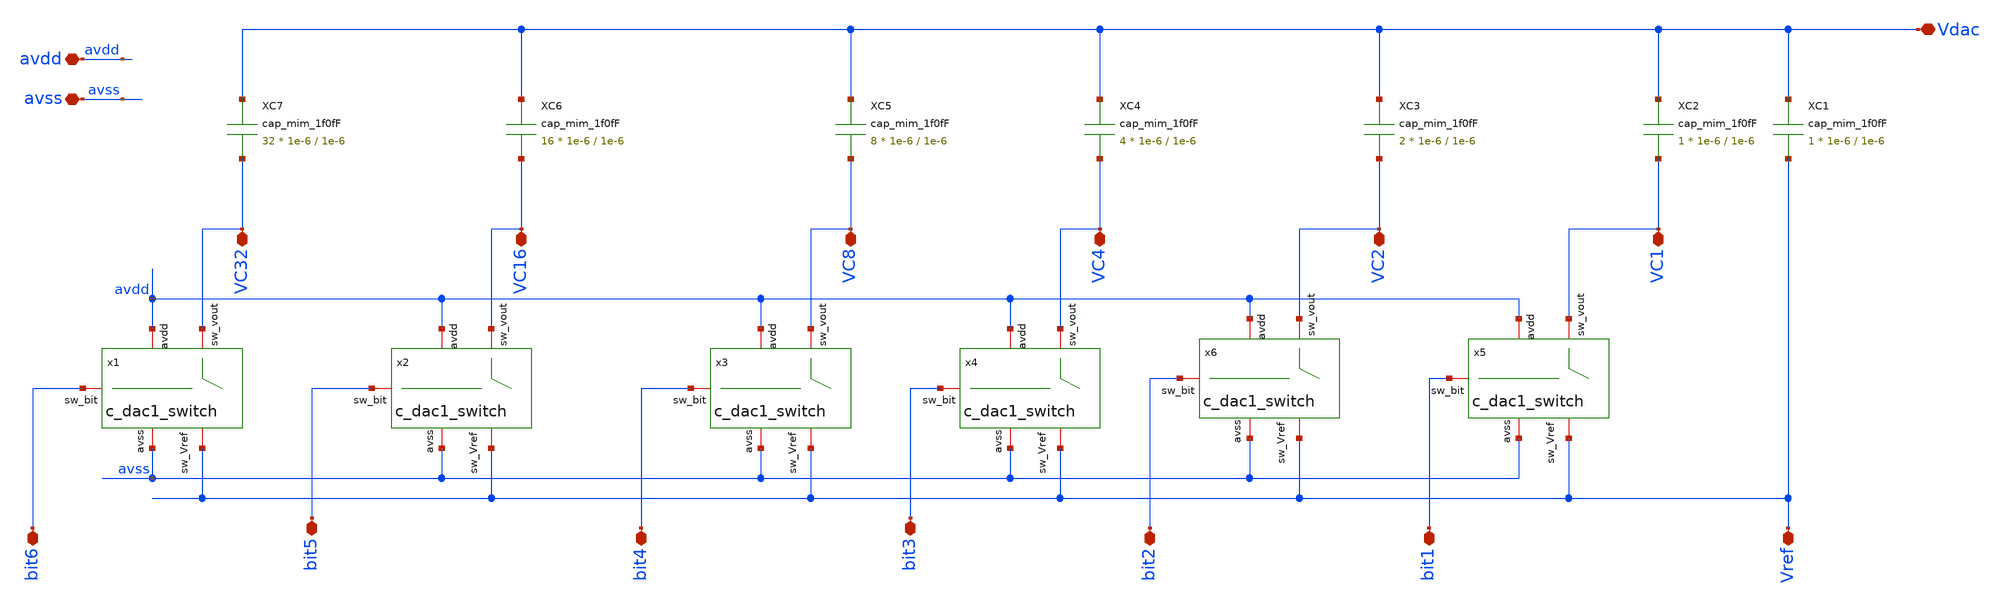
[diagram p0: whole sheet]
** sch_path: designs/libs/WK_Kadam/c_dac_v1.sch
**.subckt c_dac_v1 Vref VC1 VC2 VC4 VC8 VC16 VC32 Vdac avdd avss bit6 bit5 bit4 bit3 bit2 bit1
*.iopin Vref
*.iopin VC1
*.iopin VC2
*.iopin VC4
*.iopin VC8
*.iopin VC16
*.iopin VC32
*.iopin Vdac
*.iopin avdd
*.iopin avss
*.iopin bit6
*.iopin bit5
*.iopin bit4
*.iopin bit3
*.iopin bit2
*.iopin bit1
XC1 Vdac Vref cap_mim_1f0fF c_width=1e-6 c_length=1e-6 m=1
XC2 Vdac VC1 cap_mim_1f0fF c_width=1e-6 c_length=1e-6 m=1
XC3 Vdac VC2 cap_mim_1f0fF c_width=1e-6 c_length=1e-6 m=2
XC4 Vdac VC4 cap_mim_1f0fF c_width=1e-6 c_length=1e-6 m=4
XC5 Vdac VC8 cap_mim_1f0fF c_width=1e-6 c_length=1e-6 m=8
XC6 Vdac VC16 cap_mim_1f0fF c_width=1e-6 c_length=1e-6 m=16
XC7 Vdac VC32 cap_mim_1f0fF c_width=1e-6 c_length=1e-6 m=32
x1 avdd avss VC32 bit6 Vref c_dac1_switch
x2 avdd avss VC16 bit5 Vref c_dac1_switch
x3 avdd avss VC8 bit4 Vref c_dac1_switch
x4 avdd avss VC4 bit3 Vref c_dac1_switch
x5 avdd avss VC1 bit1 Vref c_dac1_switch
x6 avdd avss VC2 bit2 Vref c_dac1_switch
**.ends

* expanding   symbol:  Wk_Chip_Odyssey/designs/libs/WK_Kadam/c_dac1_switch.sym # of pins=5
** sym_path: designs/libs/WK_Kadam/c_dac1_switch.sym
** sch_path: designs/libs/WK_Kadam/c_dac1_switch.sch
.subckt c_dac1_switch avdd avss sw_vout sw_bit sw_Vref
*.iopin avdd
*.iopin avss
*.iopin sw_bit
*.iopin sw_vout
*.iopin sw_Vref
XM1 sw_vout sw_bit sw_Vref avss nfet_03v3 L=0.28u W=2u nf=1 ad='int((nf+1)/2) * W/nf * 0.18u' as='int((nf+2)/2) * W/nf * 0.18u'
+ pd='2*int((nf+1)/2) * (W/nf + 0.18u)' ps='2*int((nf+2)/2) * (W/nf + 0.18u)' nrd='0.18u / W' nrs='0.18u / W'
+ sa=0 sb=0 sd=0 m=1
XM3 sw_vout net1 avss avss nfet_03v3 L=0.28u W=2u nf=1 ad='int((nf+1)/2) * W/nf * 0.18u' as='int((nf+2)/2) * W/nf * 0.18u'
+ pd='2*int((nf+1)/2) * (W/nf + 0.18u)' ps='2*int((nf+2)/2) * (W/nf + 0.18u)' nrd='0.18u / W' nrs='0.18u / W'
+ sa=0 sb=0 sd=0 m=1
XM4 avss sw_bit sw_vout avdd pfet_03v3 L=0.28u W=2u nf=1 ad='int((nf+1)/2) * W/nf * 0.18u' as='int((nf+2)/2) * W/nf * 0.18u'
+ pd='2*int((nf+1)/2) * (W/nf + 0.18u)' ps='2*int((nf+2)/2) * (W/nf + 0.18u)' nrd='0.18u / W' nrs='0.18u / W'
+ sa=0 sb=0 sd=0 m=1
x1 avdd sw_bit net1 avss inv_test
XM2 sw_Vref net1 sw_vout avdd pfet_03v3 L=0.28u W=2u nf=1 ad='int((nf+1)/2) * W/nf * 0.18u' as='int((nf+2)/2) * W/nf * 0.18u'
+ pd='2*int((nf+1)/2) * (W/nf + 0.18u)' ps='2*int((nf+2)/2) * (W/nf + 0.18u)' nrd='0.18u / W' nrs='0.18u / W'
+ sa=0 sb=0 sd=0 m=1
.ends


* expanding   symbol:  Wk_Chip_Odyssey/designs/libs/WK_Kadam/inv_test.sym # of pins=4
** sym_path: Wk_Chip_Odyssey/designs/libs/WK_Kadam/inv_test.sym
** sch_path: Wk_Chip_Odyssey/designs/libs/WK_Kadam/inv_test.sch
.subckt inv_test avdd in out avss
*.iopin avdd
*.iopin avss
*.iopin in
*.iopin out
XM3 out in avss avss nfet_03v3 L=0.28u W=1u nf=1 ad='int((nf+1)/2) * W/nf * 0.18u' as='int((nf+2)/2) * W/nf * 0.18u'
+ pd='2*int((nf+1)/2) * (W/nf + 0.18u)' ps='2*int((nf+2)/2) * (W/nf + 0.18u)' nrd='0.18u / W' nrs='0.18u / W'
+ sa=0 sb=0 sd=0 m=1
XM4 out in avdd avdd pfet_03v3 L=0.28u W=2.5u nf=1 ad='int((nf+1)/2) * W/nf * 0.18u' as='int((nf+2)/2) * W/nf * 0.18u'
+ pd='2*int((nf+1)/2) * (W/nf + 0.18u)' ps='2*int((nf+2)/2) * (W/nf + 0.18u)' nrd='0.18u / W' nrs='0.18u / W'
+ sa=0 sb=0 sd=0 m=1
.ends

.end
